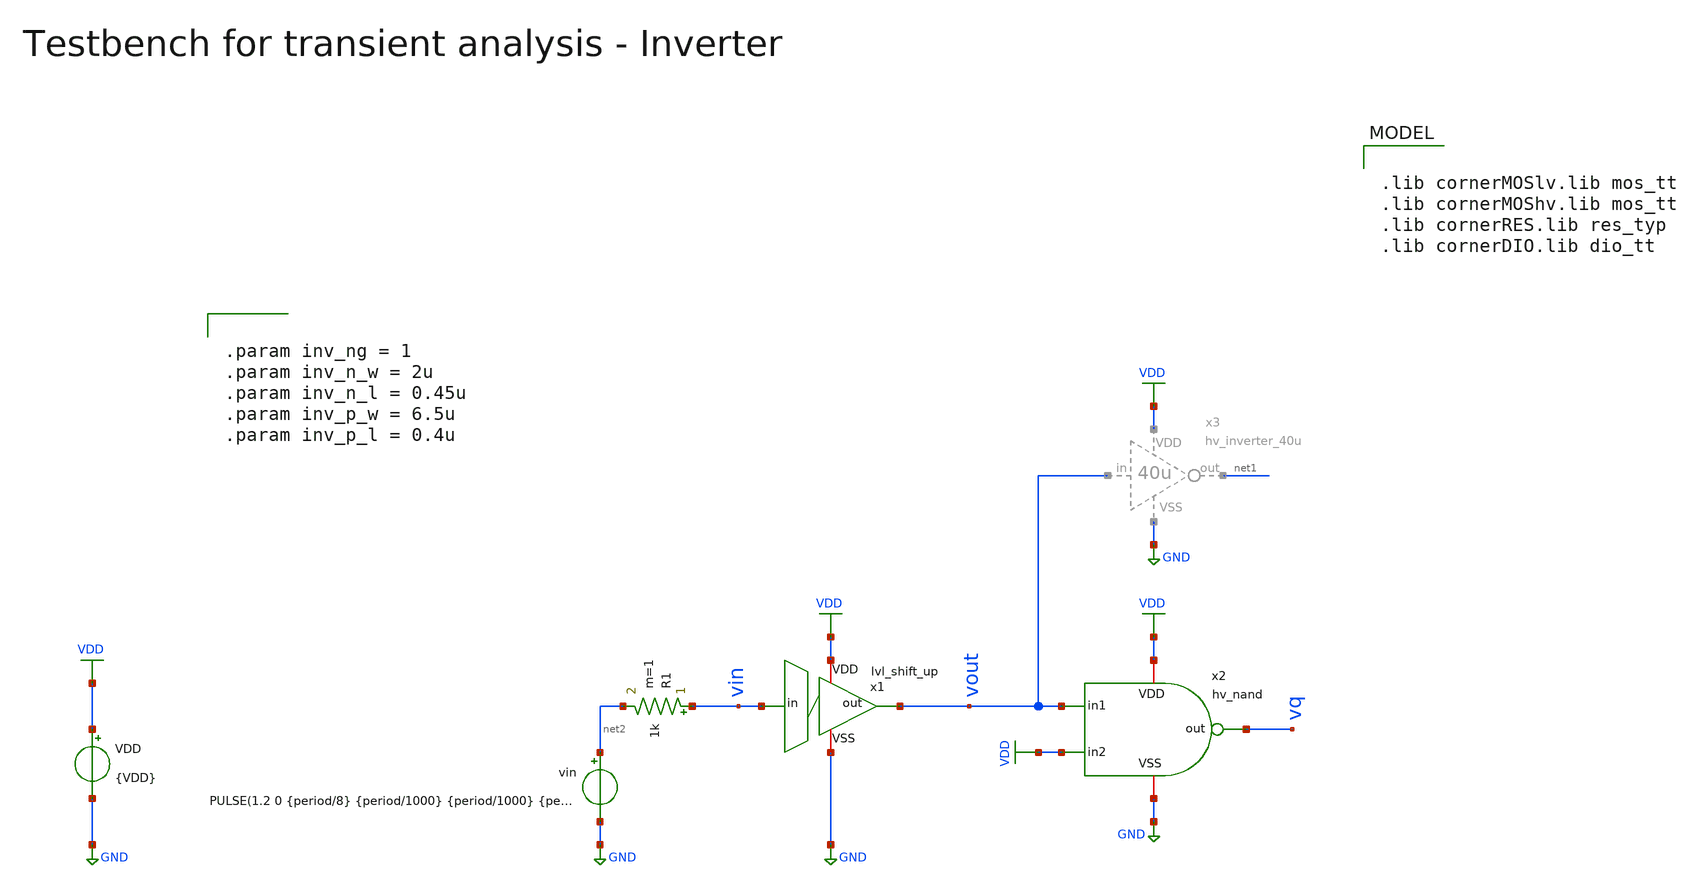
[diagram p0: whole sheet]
** sch_path: macros/heichips26_vcr/macros/switched_capacitor/testbenches/xschem/tb_lvl_shift_up_tran.sch
**.subckt tb_lvl_shift_up_tran
VDD VDD GND {VDD}
x2 VDD vout vq VDD GND hv_nand
vin net2 GND PULSE(1.2 0 {period/8} {period/1000} {period/1000} {period/2} {period})
x1 VDD vin vout GND lvl_shift_up
R1 vin net2 1k m=1
**** begin user architecture code


.param VDD=3.3
.csparam VDD=VDD
.param Vcm=VDD/2
.param temp=27
.param Cload=10p
.param Rload=1k

.param period = 2n
.csparam tstop  = {1*period}
.csparam tstep  = {period/100}

.param vth = 1.65
.param vpp = {period*2.65e+6}
.param vmax = {vth+vpp/2}
.param vmin = {vth-vpp/2}

.ic v(vq) = 0

.options savecurrents klu method=gear reltol=1e-4 abstol=1e-15 gmin=1e-15
.control

save all

* Operating Point Analysis
op
remzerovec
write @schname\.raw
set appendwrite

* Transient Analysis
tran {$&tstep} {$&tstop}
write @schname\.raw

* Plotting
plot vin+4 vout vq+4
*plot vin1+4 50*(vin2-vin1)+4+vin1 vout vq+4
*plot vin1+4 vin2+4 vq+4 vout

* Write Data
unset appendwrite
set wr_vecnames
set wr_singlescale
*wrdata ../plot_simulations/data/@schname\.txt v(vin1) v(vin2) v(vout)

*quit
.endc



.lib cornerMOSlv.lib mos_tt
.lib cornerMOShv.lib mos_tt
.lib cornerRES.lib res_typ
.lib cornerDIO.lib dio_tt



.param inv_ng = 1
.param inv_n_w = 2u
.param inv_n_l = 0.45u
.param inv_p_w = 6.5u
.param inv_p_l = 0.4u


**** end user architecture code
**.ends

* expanding   symbol:  hv_inverter_40u.sym # of pins=4
** sym_path: macros/heichips26_vcr/macros/switched_capacitor/schematic/xschem/hv_inverter_40u.sym
** sch_path: macros/heichips26_vcr/macros/switched_capacitor/schematic/xschem/hv_inverter_40u.sch
.subckt hv_inverter_40u VDD in out VSS
*.ipin in
*.iopin VDD
*.iopin VSS
*.opin out
XM2 out in VSS VSS sg13_hv_nmos w={n_w} l={n_l} ng={ng} m=1 mm_ok=1
XM3 out in VDD VDD sg13_hv_pmos w={p_w} l={p_l} ng={ng} m=1 mm_ok=1
**** begin user architecture code


.param w   = 10u
.param ng  = 4
.param n_ng = ng
.param n_w = {3u*n_ng}
.param n_l = 0.45u
.param p_ng = ng
.param p_w = {10u*p_ng}
.param p_l = 0.4u


**** end user architecture code
.ends


* expanding   symbol:  hv_nand.sym # of pins=5
** sym_path: macros/heichips26_vcr/macros/switched_capacitor/schematic/xschem/hv_nand.sym
** sch_path: macros/heichips26_vcr/macros/switched_capacitor/schematic/xschem/hv_nand.sch
.subckt hv_nand VDD in1 out in2 VSS
*.ipin in1
*.iopin VDD
*.iopin VSS
*.opin out
*.ipin in2
**** begin user architecture code


.param w   = 10u
.param ng  = 4
.param n_ng = ng
.param n_w = {3u*n_ng}
.param n_l = 0.45u
.param p_ng = ng
.param p_w = {10u*p_ng}
.param p_l = 0.4u


**** end user architecture code
XM2 out in1 net1 VSS sg13_hv_nmos w={n_w} l={n_l} ng={ng} m=1 mm_ok=1
XM3 out in2 VDD VDD sg13_hv_pmos w={p_w} l={p_l} ng={ng} m=1 mm_ok=1
XM1 net1 in2 VSS VSS sg13_hv_nmos w={n_w} l={n_l} ng={ng} m=1 mm_ok=1
XM4 out in1 VDD VDD sg13_hv_pmos w={p_w} l={p_l} ng={ng} m=1 mm_ok=1
.ends


* expanding   symbol:  lvl_shift_up.sym # of pins=4
** sym_path: macros/heichips26_vcr/macros/switched_capacitor/schematic/xschem/lvl_shift_up.sym
** sch_path: macros/heichips26_vcr/macros/switched_capacitor/schematic/xschem/lvl_shift_up.sch
.subckt lvl_shift_up VDD in out VSS
*.ipin in
*.iopin VDD
*.iopin VSS
*.opin out
XM1 net1 in VSS VSS sg13_hv_nmos w={n_ng*n_w} l={n_l} ng={n_ng} m=1 mm_ok=1
XM2 net1 in VDD VDD sg13_hv_pmos w={p_ng*p_w} l={p_l} ng={n_ng} m=1 mm_ok=1
**** begin user architecture code


.param n_ng = 2
.param n_w = 10u
.param n_l = 0.45u
.param p_ng = 2
.param p_w = 1u
.param p_l = 0.45u


**** end user architecture code
x4 VDD net1 out VSS hv_inverter_6u5
.ends


* expanding   symbol:  hv_inverter_6u5.sym # of pins=4
** sym_path: macros/heichips26_vcr/macros/switched_capacitor/schematic/xschem/hv_inverter_6u5.sym
** sch_path: macros/heichips26_vcr/macros/switched_capacitor/schematic/xschem/hv_inverter_6u5.sch
.subckt hv_inverter_6u5 VDD in out VSS
*.ipin in
*.iopin VDD
*.iopin VSS
*.opin out
XM2 out in VSS VSS sg13_hv_nmos w={n_w} l={n_l} ng={ng} m=1 mm_ok=1
XM3 out in VDD VDD sg13_hv_pmos w={p_w} l={p_l} ng={ng} m=1 mm_ok=1
**** begin user architecture code


.param ng  = 1
.param n_ng = ng
.param n_w = {2u*n_ng}
.param n_l = 0.45u
.param p_ng = ng
.param p_w = {6.5u*p_ng}
.param p_l = 0.4u


**** end user architecture code
.ends

.GLOBAL GND
.GLOBAL VDD
.end
